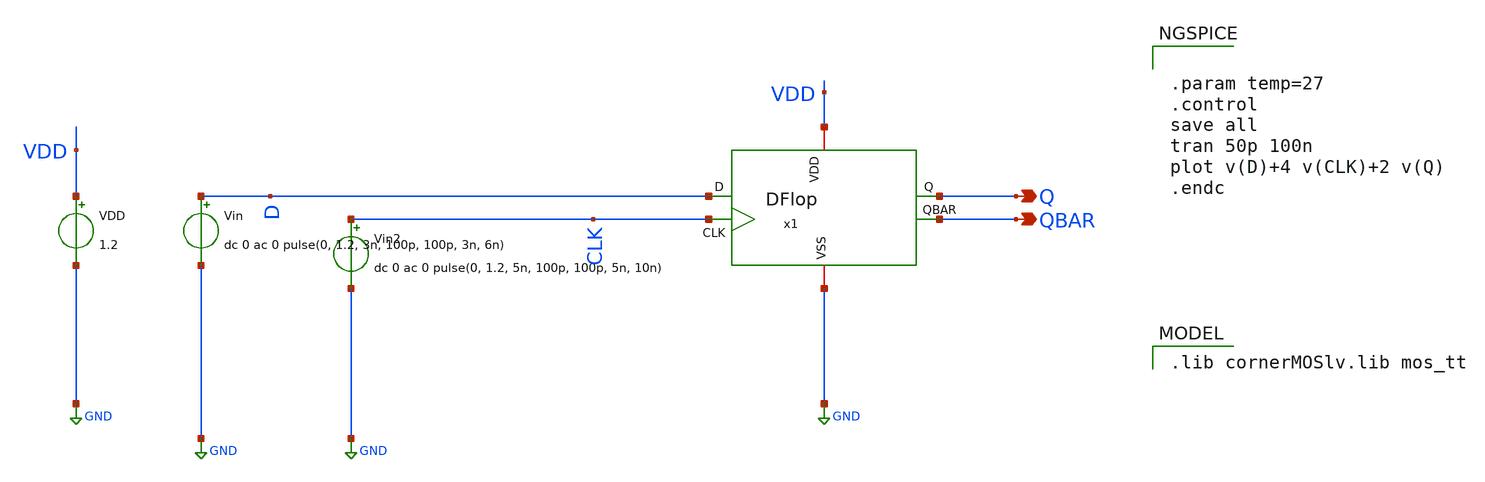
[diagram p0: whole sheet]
** sch_path: Team Designs/Team 1 Design/design_data/xschem/DFlop/DFlop_tb.sch
**.subckt DFlop_tb Q QBAR
*.opin Q
*.opin QBAR
VDD VDD GND 1.2
Vin D GND dc 0 ac 0 pulse(0, 1.2, 3n, 100p, 100p, 3n, 6n)
Vin2 CLK GND dc 0 ac 0 pulse(0, 1.2, 5n, 100p, 100p, 5n, 10n)
x1 VDD D Q CLK QBAR GND DFlop
**** begin user architecture code
 .lib cornerMOSlv.lib mos_tt



.param temp=27
.control
save all
tran 50p 100n
plot v(D)+4 v(CLK)+2 v(Q)
.endc


**** end user architecture code
**.ends
.GLOBAL GND
.end
